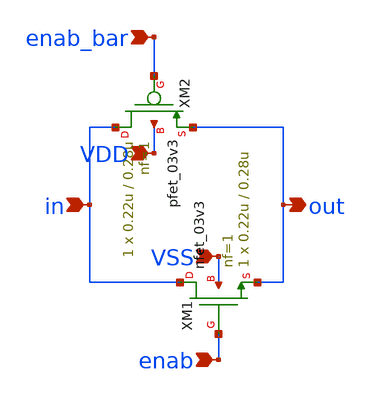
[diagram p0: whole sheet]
** sch_path: designs/libs/untitled.sch
**.subckt untitled out in VSS VDD enab_bar enab
*.opin out
*.ipin in
*.ipin VSS
*.ipin VDD
*.ipin enab_bar
*.ipin enab
XM1 in enab out VSS nfet_03v3 L=0.28u W=0.22u nf=1 ad='int((nf+1)/2) * W/nf * 0.18u' as='int((nf+2)/2) * W/nf * 0.18u'
+ pd='2*int((nf+1)/2) * (W/nf + 0.18u)' ps='2*int((nf+2)/2) * (W/nf + 0.18u)' nrd='0.18u / W' nrs='0.18u / W'
+ sa=0 sb=0 sd=0 m=1
XM2 in enab_bar out VDD pfet_03v3 L=0.28u W=0.22u nf=1 ad='int((nf+1)/2) * W/nf * 0.18u' as='int((nf+2)/2) * W/nf * 0.18u'
+ pd='2*int((nf+1)/2) * (W/nf + 0.18u)' ps='2*int((nf+2)/2) * (W/nf + 0.18u)' nrd='0.18u / W' nrs='0.18u / W'
+ sa=0 sb=0 sd=0 m=1
**.ends
.end
